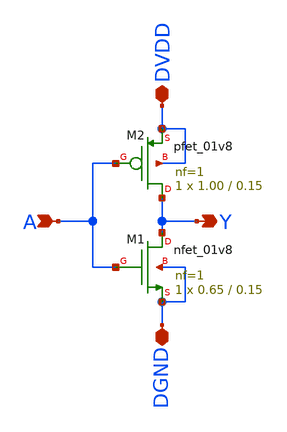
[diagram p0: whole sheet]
** sch_path: project/sch_sym_files/inv.sch
**.subckt inv Y A DVDD DGND
*.opin Y
*.ipin A
*.iopin DVDD
*.iopin DGND
XM2 Y A DVDD DVDD sky130_fd_pr__pfet_01v8 L=0.15 W=1.00 nf=1 ad='int((nf+1)/2) * W/nf * 0.29' as='int((nf+2)/2) * W/nf * 0.29'
+ pd='2*int((nf+1)/2) * (W/nf + 0.29)' ps='2*int((nf+2)/2) * (W/nf + 0.29)' nrd='0.29 / W' nrs='0.29 / W'
+ sa=0 sb=0 sd=0 mult=1 m=1
XM1 Y A DGND DGND sky130_fd_pr__nfet_01v8 L=0.15 W=0.65 nf=1 ad='int((nf+1)/2) * W/nf * 0.29' as='int((nf+2)/2) * W/nf * 0.29'
+ pd='2*int((nf+1)/2) * (W/nf + 0.29)' ps='2*int((nf+2)/2) * (W/nf + 0.29)' nrd='0.29 / W' nrs='0.29 / W'
+ sa=0 sb=0 sd=0 mult=1 m=1
**.ends
.end
